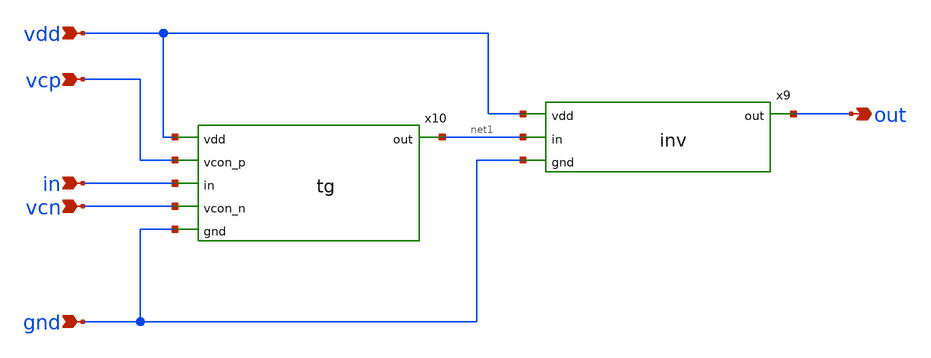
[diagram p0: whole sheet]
** sch_path: xschem/delaycell_vcro.sch
**.subckt delaycell_vcro vdd vcp in vcn gnd out
*.ipin vdd
*.ipin vcp
*.ipin in
*.ipin vcn
*.ipin gnd
*.opin out
x9 vdd net1 out gnd inv
x10 vdd vcp net1 in vcn gnd tg
**.ends
.end
